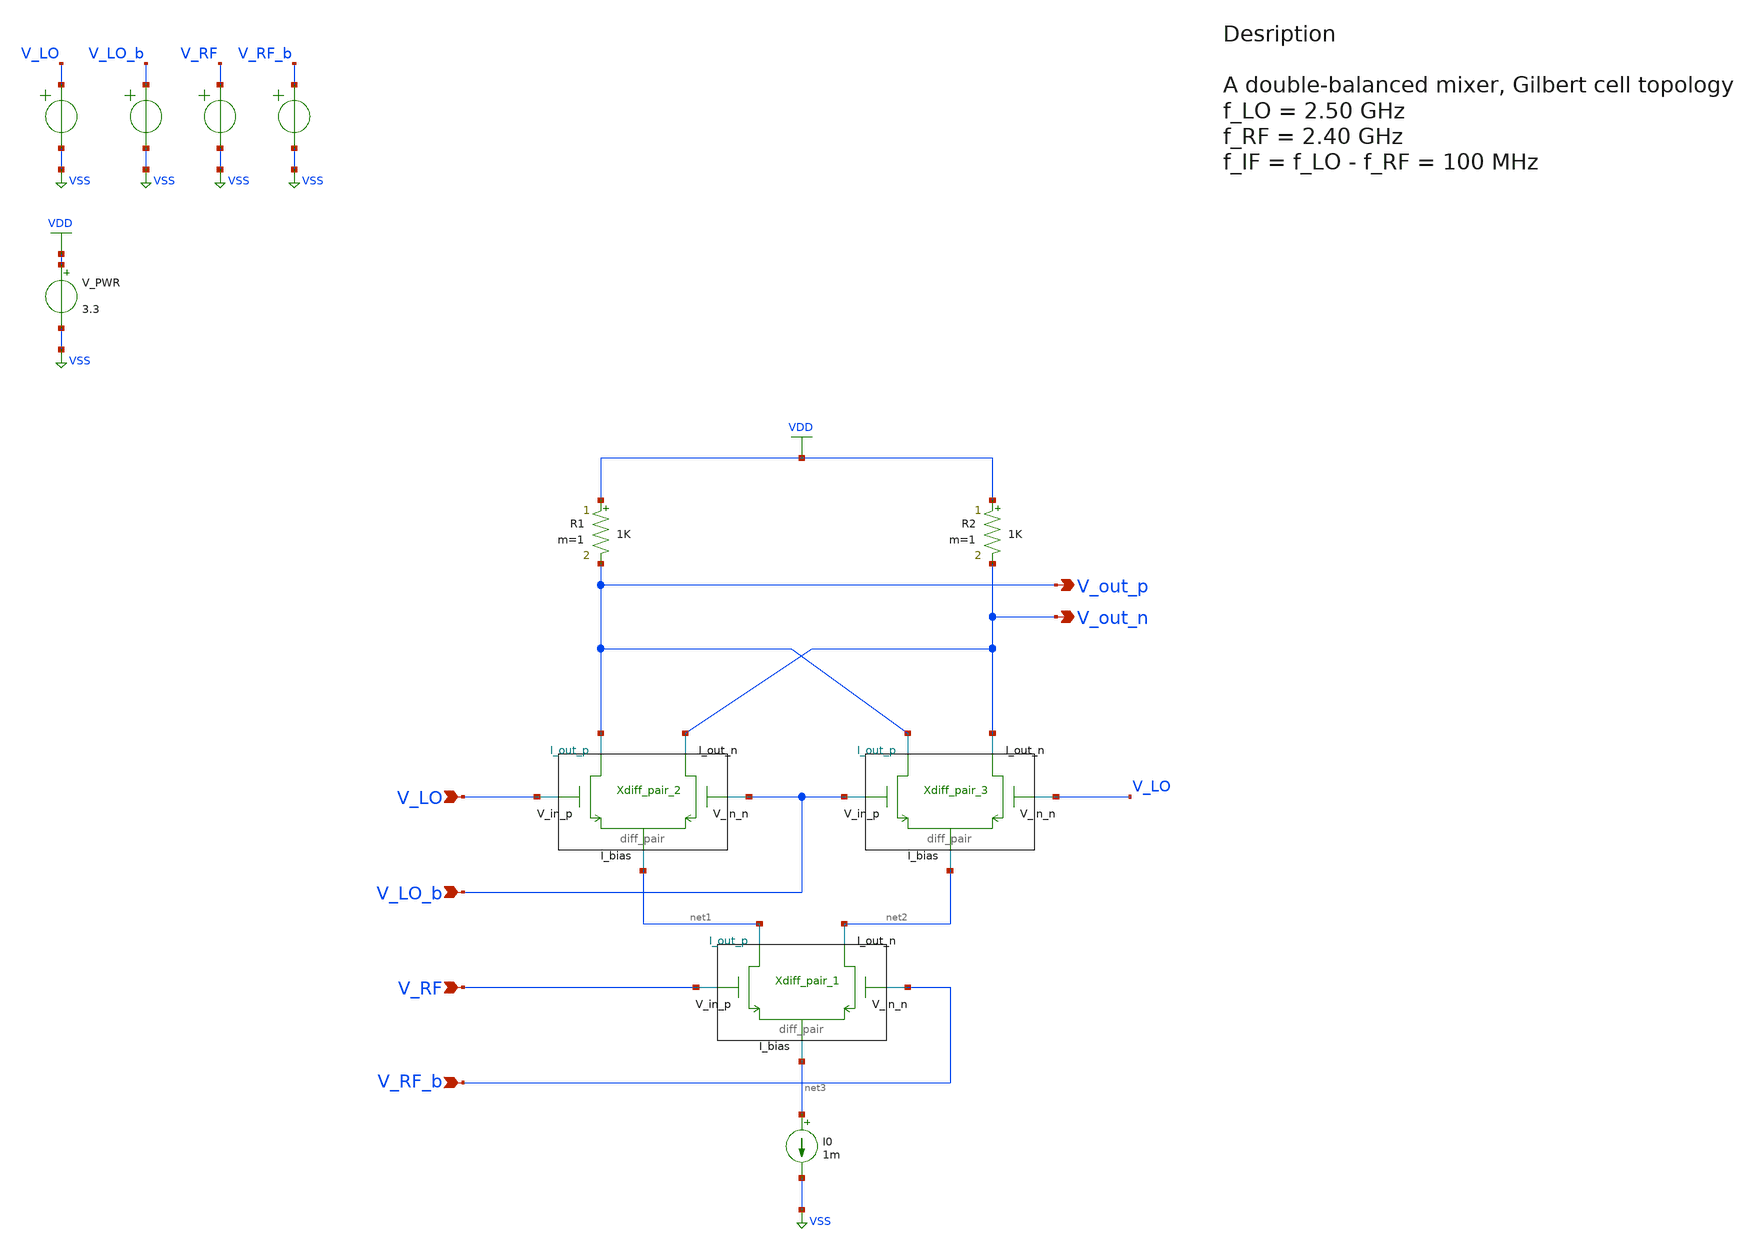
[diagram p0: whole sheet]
** sch_path: src/design_xsch/Gilbert_cell.sch
**.subckt Gilbert_cell V_LO V_LO_b V_RF V_RF_b V_out_p V_out_n
*.ipin V_LO
*.ipin V_LO_b
*.ipin V_RF
*.ipin V_RF_b
*.opin V_out_p
*.opin V_out_n
I0 net3 VSS 1m
E1 V_LO VSS VOL=' '1.5 + sin(time * 2.5 * 1e9)' '
E2 V_LO_b VSS VOL=' '1.5 - sin(time * 2.5 * 1e9)' '
E4 V_RF VSS VOL=' '1.5 + sin(time * 2.40 * 1e9)' '
E6 V_RF_b VSS VOL=' '1.5 - sin(time * 2.40 * 1e9)' '
Xdiff_pair_1 net2 net1 V_RF V_RF_b net3 VSS diff_pair W_neg=0.22u L_neg=0.28u W_pos=2u L_pos=0.28u
+ m=1
Xdiff_pair_2 V_out_n V_out_p V_LO V_LO_b net1 VSS diff_pair W_neg=0.22u L_neg=0.28u W_pos=0.22u
+ L_pos=0.28u m=1
Xdiff_pair_3 V_out_n V_out_p V_LO_b V_LO net2 VSS diff_pair W_neg=0.22u L_neg=0.28u W_pos=0.22u
+ L_pos=0.28u m=1
R1 VDD V_out_p 1K m=1
R2 VDD V_out_n 1K m=1
V_PWR VDD VSS 3.3
.save i(v_pwr)
**** begin user architecture code

.include $::180MCU_MODELS/design.ngspice
.lib $::180MCU_MODELS/sm141064.ngspice typical



.temp 27
.control
save all
tran 10p 100n
write Gilbert_sim.raw
.endc


**** end user architecture code
**.ends

* expanding   symbol:  /home/vasil/Downloads/SSCS_PICO_2025/src/design_xsch/diff_pair.sym # of
*+ pins=5
** sym_path: src/design_xsch/diff_pair.sym
** sch_path: src/design_xsch/diff_pair.sch
.subckt diff_pair I_out_n I_out_p V_in_p V_in_n I_bias VSSPIN  mult=1  W_neg=0.22u L_neg=0.28u
+ W_pos=0.22u L_pos=0.28u
*.ipin V_in_p
*.ipin V_in_n
*.iopin I_out_p
*.iopin I_out_n
*.iopin I_bias
XM1 I_out_p V_in_p I_bias VSS nfet_03v3 L=L_pos W=W_pos nf=1 ad='int((nf+1)/2) * W/nf * 0.18u' as='int((nf+2)/2) * W/nf * 0.18u'
+ pd='2*int((nf+1)/2) * (W/nf + 0.18u)' ps='2*int((nf+2)/2) * (W/nf + 0.18u)' nrd='0.18u / W' nrs='0.18u / W'
+ sa=0 sb=0 sd=0 m=mult
XM2 I_out_n V_in_n I_bias VSS nfet_03v3 L=L_neg W=W_neg nf=1 ad='int((nf+1)/2) * W/nf * 0.18u' as='int((nf+2)/2) * W/nf * 0.18u'
+ pd='2*int((nf+1)/2) * (W/nf + 0.18u)' ps='2*int((nf+2)/2) * (W/nf + 0.18u)' nrd='0.18u / W' nrs='0.18u / W'
+ sa=0 sb=0 sd=0 m=mult
.ends

.GLOBAL VSS
.GLOBAL VDD
.end
